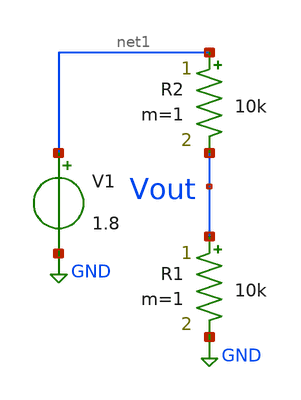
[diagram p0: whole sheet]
** sch_path: schematics/voltage_divider.sch
**.subckt voltage_divider
R1 Vout GND 10k m=1
V1 net1 GND 1.8
R2 net1 Vout 10k m=1
**** begin user architecture code


.op


**** end user architecture code
**.ends
.GLOBAL GND
.end
